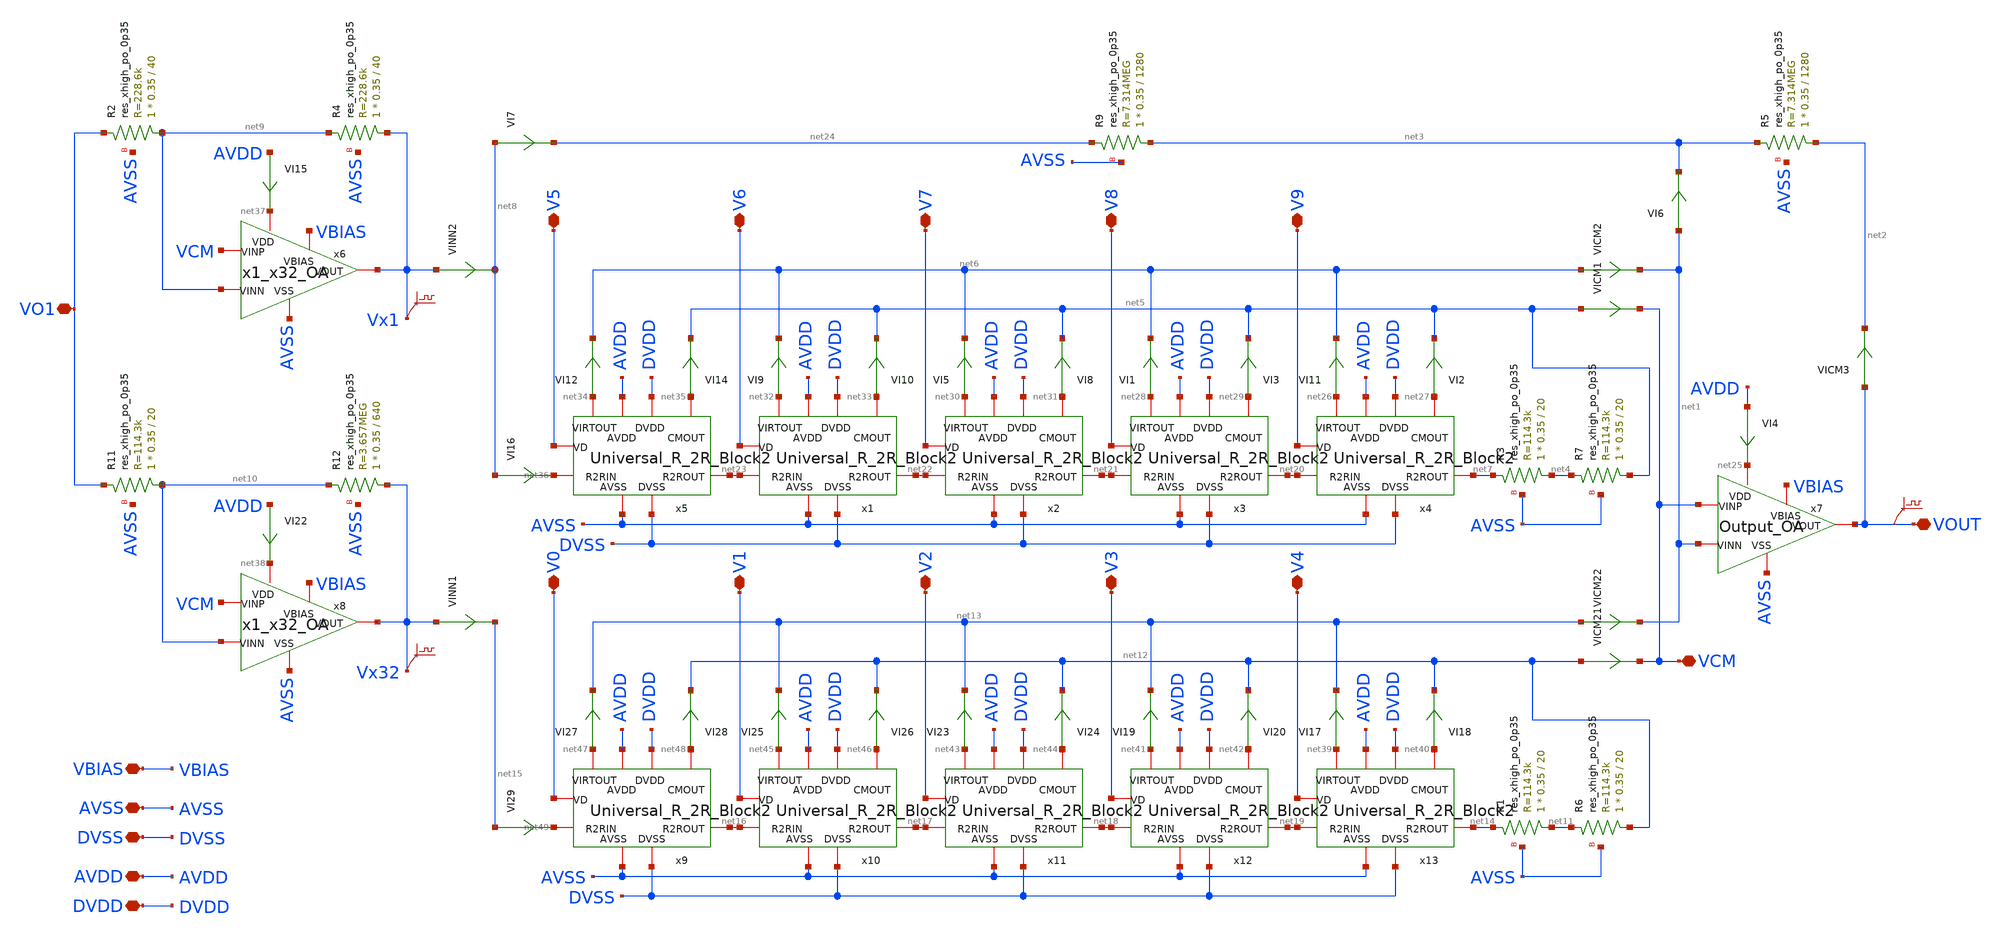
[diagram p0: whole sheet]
** sch_path: xschem/Parallel_10B_Block2.sch
**.subckt Parallel_10B_Block2 VOUT VCM VO1 V5 V6 V7 V8 V9 V0 V1 V2 V3 V4 AVSS DVSS VBIAS AVDD DVDD
*.iopin VOUT
*.iopin VCM
*.iopin VO1
*.iopin V5
*.iopin V6
*.iopin V7
*.iopin V8
*.iopin V9
*.iopin V0
*.iopin V1
*.iopin V2
*.iopin V3
*.iopin V4
*.iopin AVSS
*.iopin DVSS
*.iopin VBIAS
*.iopin AVDD
*.iopin DVDD
VI4 AVDD net25 0
.save i(vi4)
VI6 net1 net3 0
.save i(vi6)
VI7 net8 net24 0
.save i(vi7)
.save v(vout)
VI11 net26 net6 0
.save i(vi11)
VI2 net27 net5 0
.save i(vi2)
VI1 net28 net6 0
.save i(vi1)
VI3 net29 net5 0
.save i(vi3)
VICM1 net5 VCM 0
.save i(vicm1)
VICM2 net6 net1 0
.save i(vicm2)
VI5 net30 net6 0
.save i(vi5)
VI8 net31 net5 0
.save i(vi8)
VI9 net32 net6 0
.save i(vi9)
VI10 net33 net5 0
.save i(vi10)
VI12 net34 net6 0
.save i(vi12)
VI14 net35 net5 0
.save i(vi14)
VINN2 Vx1 net8 0
.save i(vinn2)
x5 V5 DVDD net34 net35 net36 net23 DVSS AVDD AVSS Universal_R_2R_Block2
x1 V6 DVDD net32 net33 net23 net22 DVSS AVDD AVSS Universal_R_2R_Block2
x2 V7 DVDD net30 net31 net22 net21 DVSS AVDD AVSS Universal_R_2R_Block2
x3 V8 DVDD net28 net29 net21 net20 DVSS AVDD AVSS Universal_R_2R_Block2
x4 V9 DVDD net26 net27 net20 net7 DVSS AVDD AVSS Universal_R_2R_Block2
VI15 AVDD net37 0
.save i(vi15)
VI16 net8 net36 0
.save i(vi16)
.save v(vx1)
VI22 AVDD net38 0
.save i(vi22)
.save v(vx32)
VICM3 VOUT net2 0
.save i(vicm3)
VI17 net39 net13 0
.save i(vi17)
VI18 net40 net12 0
.save i(vi18)
VI19 net41 net13 0
.save i(vi19)
VI20 net42 net12 0
.save i(vi20)
VICM21 net12 VCM 0
.save i(vicm21)
VICM22 net13 net1 0
.save i(vicm22)
VI23 net43 net13 0
.save i(vi23)
VI24 net44 net12 0
.save i(vi24)
VI25 net45 net13 0
.save i(vi25)
VI26 net46 net12 0
.save i(vi26)
VI27 net47 net13 0
.save i(vi27)
VI28 net48 net12 0
.save i(vi28)
x9 V0 DVDD net47 net48 net49 net16 DVSS AVDD AVSS Universal_R_2R_Block2
x10 V1 DVDD net45 net46 net16 net17 DVSS AVDD AVSS Universal_R_2R_Block2
x11 V2 DVDD net43 net44 net17 net18 DVSS AVDD AVSS Universal_R_2R_Block2
x12 V3 DVDD net41 net42 net18 net19 DVSS AVDD AVSS Universal_R_2R_Block2
x13 V4 DVDD net39 net40 net19 net14 DVSS AVDD AVSS Universal_R_2R_Block2
VI29 net15 net49 0
.save i(vi29)
VINN1 Vx32 net15 0
.save i(vinn1)
x7 net25 VOUT net1 VCM VBIAS AVSS Output_OA
x6 net37 Vx1 net9 VCM VBIAS AVSS x1_x32_OA
x8 net38 Vx32 net10 VCM VBIAS AVSS x1_x32_OA
XR11 net10 VO1 AVSS sky130_fd_pr__res_xhigh_po_0p35 L=20 mult=1 m=1
XR12 Vx32 net10 AVSS sky130_fd_pr__res_xhigh_po_0p35 L=640 mult=1 m=1
XR2 net9 VO1 AVSS sky130_fd_pr__res_xhigh_po_0p35 L=40 mult=1 m=1
XR4 Vx1 net9 AVSS sky130_fd_pr__res_xhigh_po_0p35 L=40 mult=1 m=1
XR9 net3 net24 AVSS sky130_fd_pr__res_xhigh_po_0p35 L=1280 mult=1 m=1
XR5 net2 net3 AVSS sky130_fd_pr__res_xhigh_po_0p35 L=1280 mult=1 m=1
XR6 net12 net11 AVSS sky130_fd_pr__res_xhigh_po_0p35 L=20 mult=1 m=1
XR1 net11 net14 AVSS sky130_fd_pr__res_xhigh_po_0p35 L=20 mult=1 m=1
XR3 net4 net7 AVSS sky130_fd_pr__res_xhigh_po_0p35 L=20 mult=1 m=1
XR7 net5 net4 AVSS sky130_fd_pr__res_xhigh_po_0p35 L=20 mult=1 m=1
**.ends
.end
